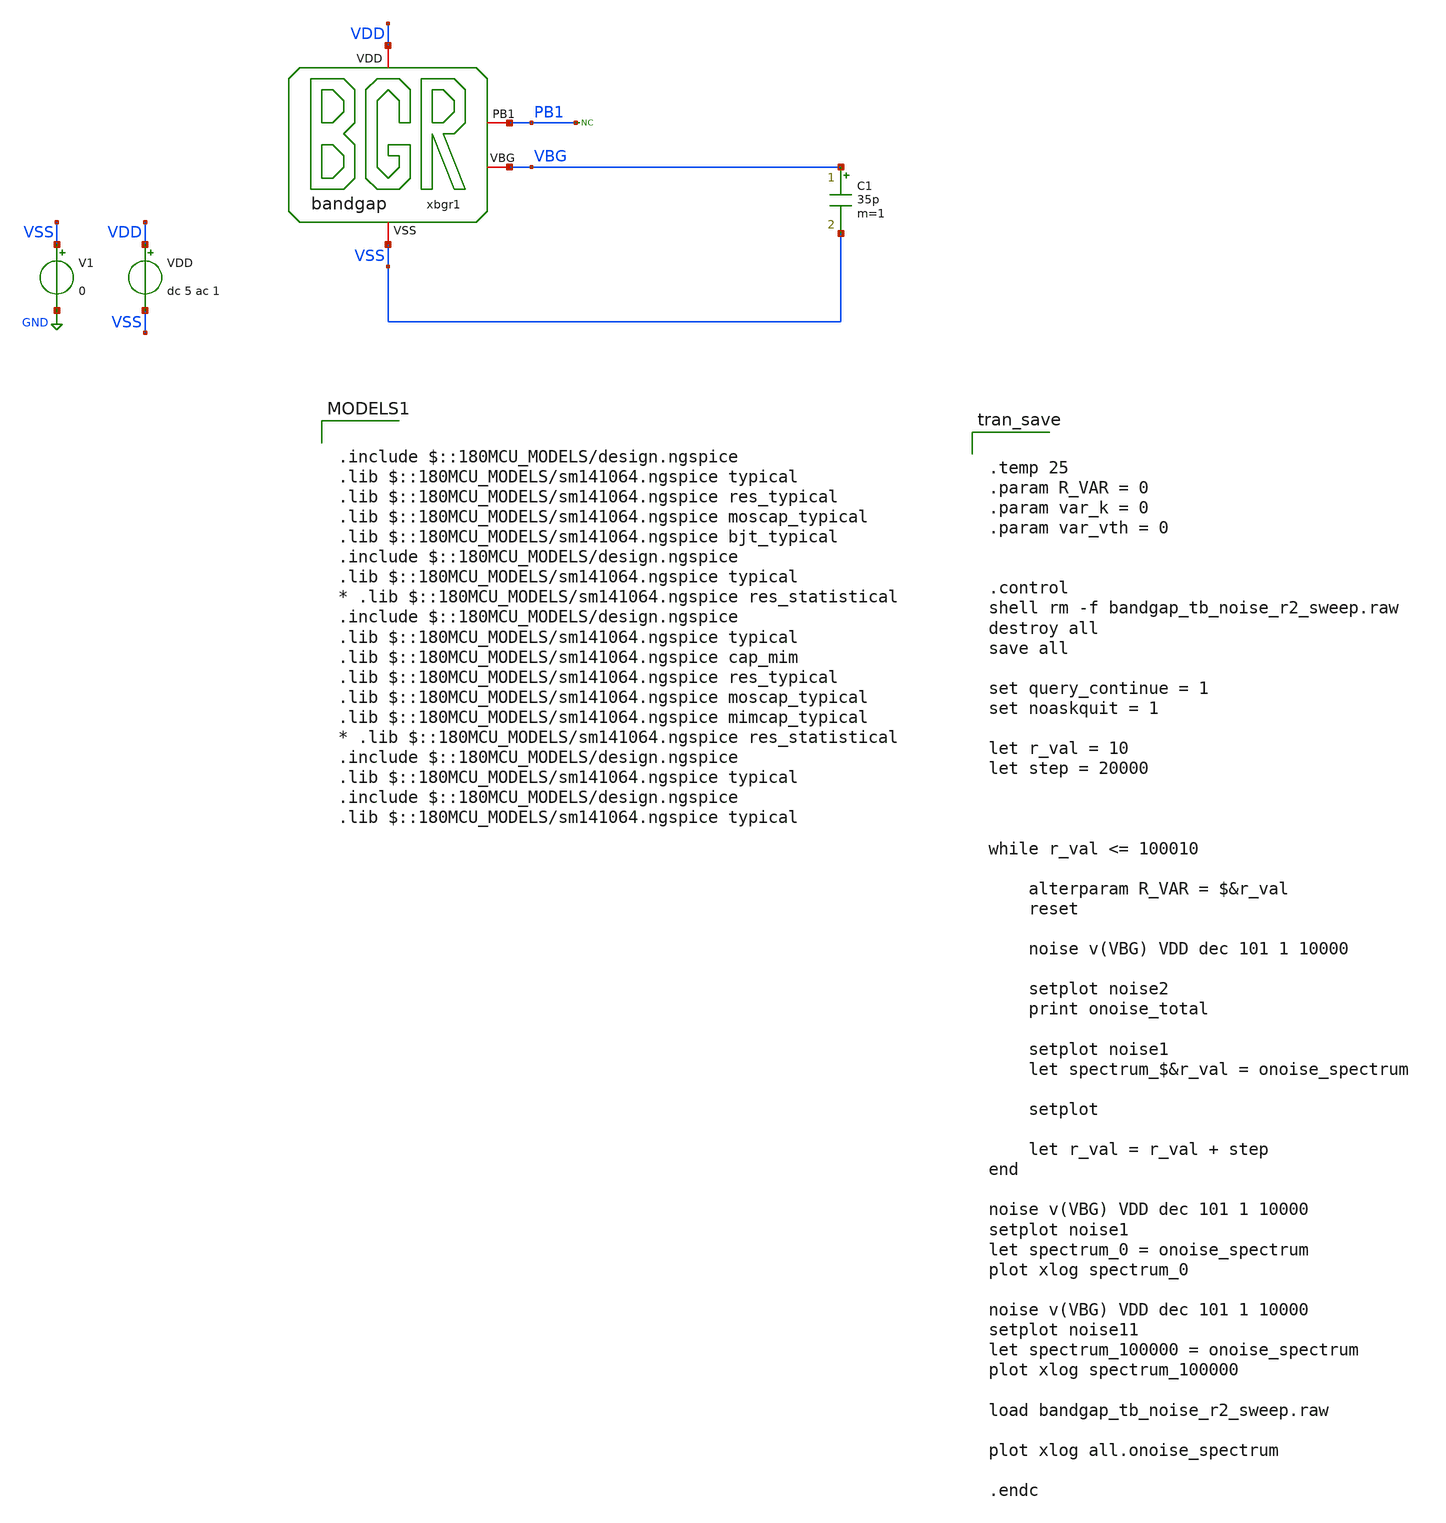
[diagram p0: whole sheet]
** sch_path: bandgap/xschem/sim/bandgap_tb_noise_r2_sweep.sch
**.subckt bandgap_tb_noise_r2_sweep
V1 VSS GND 0
VDD VDD VSS dc 5 ac 1
xbgr1 VDD PB1 VBG VSS bandgap
* noconn PB1
C1 VBG VSS 35p m=1
**** begin user architecture code


.temp 25
.param R_VAR = 0
.param var_k = 0
.param var_vth = 0


.control
shell rm -f bandgap_tb_noise_r2_sweep.raw
destroy all
save all

set query_continue = 1
set noaskquit = 1

let r_val = 10
let step = 20000



while r_val <= 100010

    alterparam R_VAR = $&r_val
    reset

    noise v(VBG) VDD dec 101 1 10000

    setplot noise2
    print onoise_total

    setplot noise1
    let spectrum_$&r_val = onoise_spectrum

    setplot

    let r_val = r_val + step
end

noise v(VBG) VDD dec 101 1 10000
setplot noise1
let spectrum_0 = onoise_spectrum
plot xlog spectrum_0

noise v(VBG) VDD dec 101 1 10000
setplot noise11
let spectrum_100000 = onoise_spectrum
plot xlog spectrum_100000

load bandgap_tb_noise_r2_sweep.raw

plot xlog all.onoise_spectrum

.endc



.include $::180MCU_MODELS/design.ngspice
.lib $::180MCU_MODELS/sm141064.ngspice typical
.lib $::180MCU_MODELS/sm141064.ngspice res_typical
.lib $::180MCU_MODELS/sm141064.ngspice moscap_typical
.lib $::180MCU_MODELS/sm141064.ngspice bjt_typical
.include $::180MCU_MODELS/design.ngspice
.lib $::180MCU_MODELS/sm141064.ngspice typical
* .lib $::180MCU_MODELS/sm141064.ngspice res_statistical
.include $::180MCU_MODELS/design.ngspice
.lib $::180MCU_MODELS/sm141064.ngspice typical
.lib $::180MCU_MODELS/sm141064.ngspice cap_mim
.lib $::180MCU_MODELS/sm141064.ngspice res_typical
.lib $::180MCU_MODELS/sm141064.ngspice moscap_typical
.lib $::180MCU_MODELS/sm141064.ngspice mimcap_typical
* .lib $::180MCU_MODELS/sm141064.ngspice res_statistical
.include $::180MCU_MODELS/design.ngspice
.lib $::180MCU_MODELS/sm141064.ngspice typical
.include $::180MCU_MODELS/design.ngspice
.lib $::180MCU_MODELS/sm141064.ngspice typical

**** end user architecture code
**.ends

* expanding   symbol:  bandgap/xschem/dev/bandgap.sym # of pins=4
** sym_path: bandgap/cace/testbenches/bandgap.sym
** sch_path: bandgap/cace/testbenches/bandgap.sch
.subckt bandgap VDD PB1 VBG VSS
*.iopin VSS
*.iopin VDD
*.iopin PB1
*.iopin VBG
R0 net7 VSET 1.7k m=1
R1 VSET VSS 7.6k m=1
R2 VB0 VBG 17000 m=1
XQ1 PB1 net8 net6 VSS npn_10p00x10p00 m=12
XQ0 VB0 VB0 net3 VSS npn_10p00x10p00 m=1
XM4 VSS net2 VSS VSS nfet_03v3 L=1u W=19u nf=1 ad='int((nf+1)/2) * W/nf * 0.18u' as='int((nf+2)/2) * W/nf * 0.18u'
+ pd='2*int((nf+1)/2) * (W/nf + 0.18u)' ps='2*int((nf+2)/2) * (W/nf + 0.18u)' nrd='0.18u / W' nrs='0.18u / W'
+ sa=0 sb=0 sd=0 m=1
XM2 net2 VSS VDD VDD pfet_03v3 L=10u W=1u nf=1 ad='int((nf+1)/2) * W/nf * 0.18u' as='int((nf+2)/2) * W/nf * 0.18u'
+ pd='2*int((nf+1)/2) * (W/nf + 0.18u)' ps='2*int((nf+2)/2) * (W/nf + 0.18u)' nrd='0.18u / W' nrs='0.18u / W'
+ sa=0 sb=0 sd=0 m=1
XM3 net5 net2 VDD VDD pfet_03v3 L=2u W=2u nf=1 ad='int((nf+1)/2) * W/nf * 0.18u' as='int((nf+2)/2) * W/nf * 0.18u'
+ pd='2*int((nf+1)/2) * (W/nf + 0.18u)' ps='2*int((nf+2)/2) * (W/nf + 0.18u)' nrd='0.18u / W' nrs='0.18u / W'
+ sa=0 sb=0 sd=0 m=1
XM1 net1 net1 VDD VDD pfet_03v3 L=7.4u W=20u nf=1 ad='int((nf+1)/2) * W/nf * 0.18u' as='int((nf+2)/2) * W/nf * 0.18u'
+ pd='2*int((nf+1)/2) * (W/nf + 0.18u)' ps='2*int((nf+2)/2) * (W/nf + 0.18u)' nrd='0.18u / W' nrs='0.18u / W'
+ sa=0 sb=0 sd=0 m=1
XM0 net4 net1 VDD VDD pfet_03v3 L=7.4u W=20u nf=1 ad='int((nf+1)/2) * W/nf * 0.18u' as='int((nf+2)/2) * W/nf * 0.18u'
+ pd='2*int((nf+1)/2) * (W/nf + 0.18u)' ps='2*int((nf+2)/2) * (W/nf + 0.18u)' nrd='0.18u / W' nrs='0.18u / W'
+ sa=0 sb=0 sd=0 m=1
VQ0E net3 VSET 0
VM0D net4 VB0 0
VM3D net5 VB0 0
VQ1E net6 net7 0
VM1D net1 PB1 0
VQ1B VBG net8 0
.ends

.GLOBAL GND
.end
